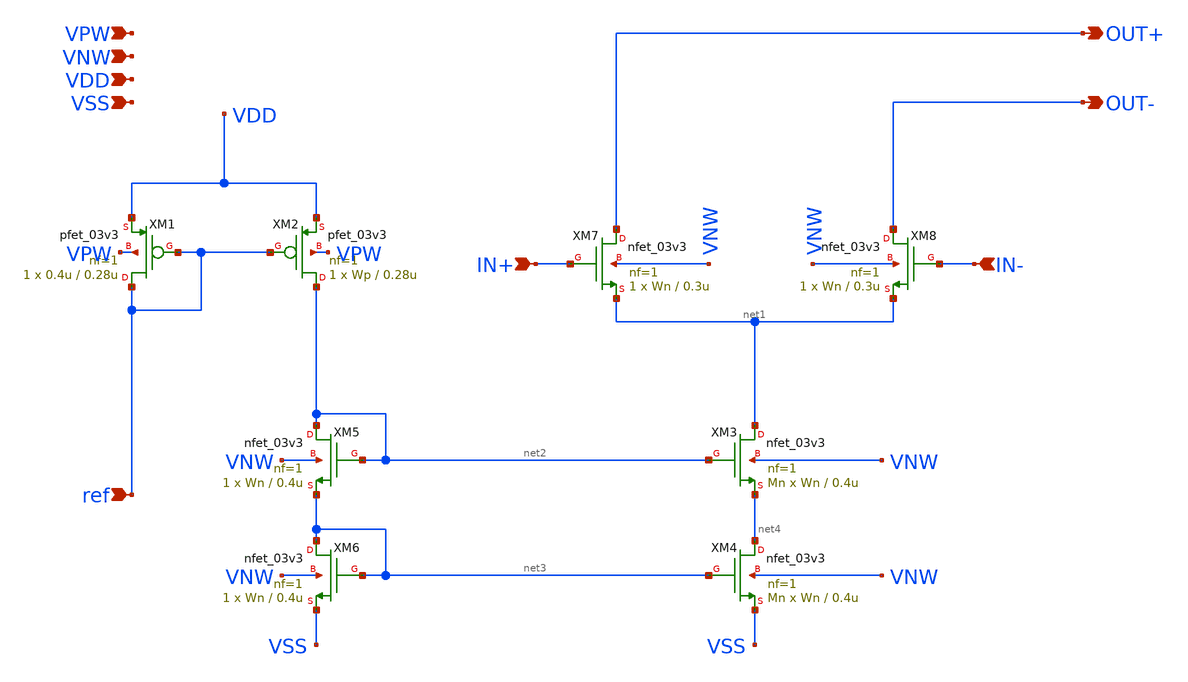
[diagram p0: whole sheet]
** sch_path: DAC/xschem/analog_cell/CCU.sch
**.subckt CCU ref IN+ IN- OUT+ OUT- VPW VNW VSS VDD
*.ipin ref
*.ipin IN+
*.ipin IN-
*.opin OUT+
*.opin OUT-
*.ipin VPW
*.ipin VNW
*.ipin VSS
*.ipin VDD
XM3 net1 net2 net4 VNW nfet_03v3 L=0.4u W=Wn nf=1 ad='int((nf+1)/2) * W/nf * 0.18u' as='int((nf+2)/2) * W/nf * 0.18u'
+ pd='2*int((nf+1)/2) * (W/nf + 0.18u)' ps='2*int((nf+2)/2) * (W/nf + 0.18u)' nrd='0.18u / W' nrs='0.18u / W'
+ sa=0 sb=0 sd=0 m=Mn
XM4 net4 net3 VSS VNW nfet_03v3 L=0.4u W=Wn nf=1 ad='int((nf+1)/2) * W/nf * 0.18u' as='int((nf+2)/2) * W/nf * 0.18u'
+ pd='2*int((nf+1)/2) * (W/nf + 0.18u)' ps='2*int((nf+2)/2) * (W/nf + 0.18u)' nrd='0.18u / W' nrs='0.18u / W'
+ sa=0 sb=0 sd=0 m=Mn
XM5 net2 net2 net3 VNW nfet_03v3 L=0.4u W=Wn nf=1 ad='int((nf+1)/2) * W/nf * 0.18u' as='int((nf+2)/2) * W/nf * 0.18u'
+ pd='2*int((nf+1)/2) * (W/nf + 0.18u)' ps='2*int((nf+2)/2) * (W/nf + 0.18u)' nrd='0.18u / W' nrs='0.18u / W'
+ sa=0 sb=0 sd=0 m=1
XM6 net3 net3 VSS VNW nfet_03v3 L=0.4u W=Wn nf=1 ad='int((nf+1)/2) * W/nf * 0.18u' as='int((nf+2)/2) * W/nf * 0.18u'
+ pd='2*int((nf+1)/2) * (W/nf + 0.18u)' ps='2*int((nf+2)/2) * (W/nf + 0.18u)' nrd='0.18u / W' nrs='0.18u / W'
+ sa=0 sb=0 sd=0 m=1
XM1 ref ref VDD VPW pfet_03v3 L=0.28u W=0.4u nf=1 ad='int((nf+1)/2) * W/nf * 0.18u' as='int((nf+2)/2) * W/nf * 0.18u'
+ pd='2*int((nf+1)/2) * (W/nf + 0.18u)' ps='2*int((nf+2)/2) * (W/nf + 0.18u)' nrd='0.18u / W' nrs='0.18u / W'
+ sa=0 sb=0 sd=0 m=1
XM2 net2 ref VDD VPW pfet_03v3 L=0.28u W=Wp nf=1 ad='int((nf+1)/2) * W/nf * 0.18u' as='int((nf+2)/2) * W/nf * 0.18u'
+ pd='2*int((nf+1)/2) * (W/nf + 0.18u)' ps='2*int((nf+2)/2) * (W/nf + 0.18u)' nrd='0.18u / W' nrs='0.18u / W'
+ sa=0 sb=0 sd=0 m=1
XM7 OUT+ IN+ net1 VNW nfet_03v3 L=0.3u W=Wn nf=1 ad='int((nf+1)/2) * W/nf * 0.18u' as='int((nf+2)/2) * W/nf * 0.18u'
+ pd='2*int((nf+1)/2) * (W/nf + 0.18u)' ps='2*int((nf+2)/2) * (W/nf + 0.18u)' nrd='0.18u / W' nrs='0.18u / W'
+ sa=0 sb=0 sd=0 m=1
XM8 OUT- IN- net1 VNW nfet_03v3 L=0.3u W=Wn nf=1 ad='int((nf+1)/2) * W/nf * 0.18u' as='int((nf+2)/2) * W/nf * 0.18u'
+ pd='2*int((nf+1)/2) * (W/nf + 0.18u)' ps='2*int((nf+2)/2) * (W/nf + 0.18u)' nrd='0.18u / W' nrs='0.18u / W'
+ sa=0 sb=0 sd=0 m=1
**.ends
.end
